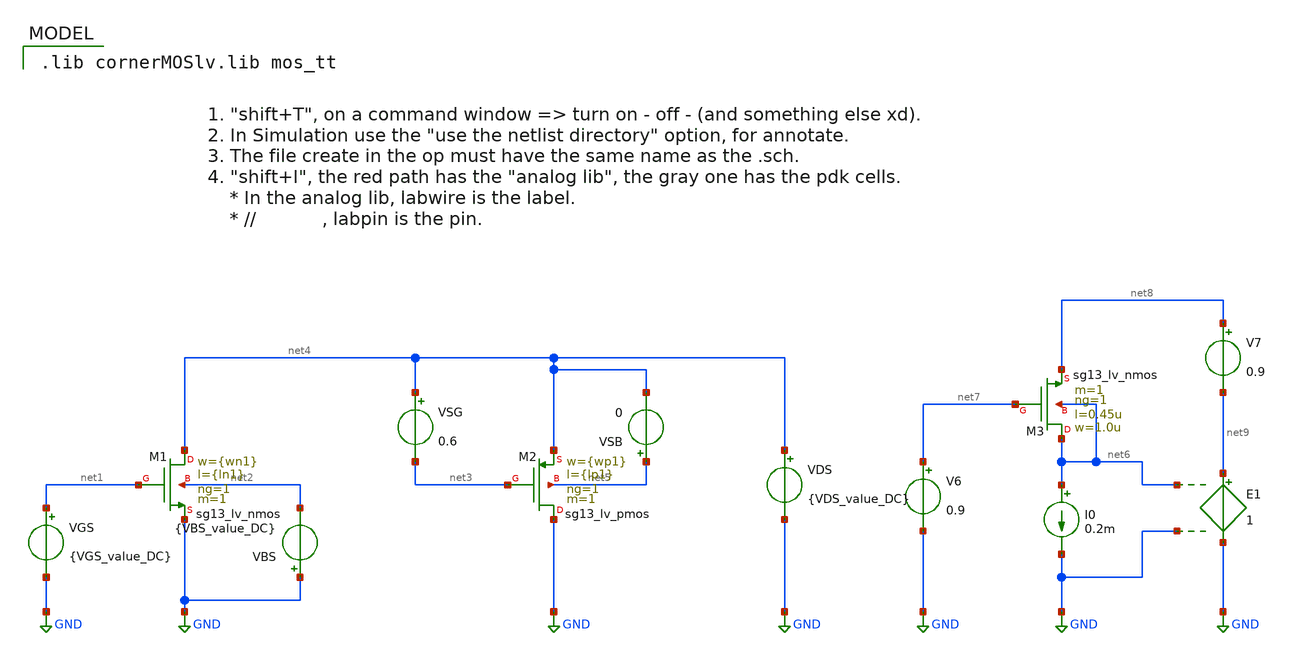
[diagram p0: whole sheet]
** sch_path: W2WDAC/W2W-DAC/CMOSCHART_sg130_lv_tb.sch
**.subckt CMOSCHART_sg130_lv_tb
VGS net1 GND {VGS_value_DC}
VDS net4 GND {VDS_value_DC}
VBS GND net2 {VBS_value_DC}
VSG net4 net3 0.6
VSB net5 net4 0
I0 net6 GND 0.2m
V6 net7 GND 0.9
V7 net8 net9 0.9
E1 net9 GND net6 GND 1
XM1 net4 net1 GND net2 sg13_lv_nmos w={wn1} l={ln1} ng=1 m=1 mm_ok=1
XM2 GND net3 net4 net5 sg13_lv_pmos w={wp1} l={lp1} ng=1 m=1 mm_ok=1
XM3 net6 net7 net8 net6 sg13_lv_nmos w=1.0u l=0.45u ng=1 m=1 mm_ok=1
**** begin user architecture code
 .lib cornerMOSlv.lib mos_tt



.option sparse
.param wp1=1u
.param lp1=0.13u
.temp 65
.param wn1=1u
.param ln1=0.13u
.param VGS_value_DC=0.6
.param VDS_value_DC=0.6
.param VBS_value_DC=0

.op
.save all
.control
option numdgt=3
set wr_singlescale
set wr_vecnames

compose wp_vec start=1.44u stop=1.46u step=0.005u
*6u 6.5u 7u 7.5u 8u 8.5u 9u 9.5u 10u 10.5u 11u 11.5u 12u 12.5u 13u 13.5u 14u 14.5u 15u 15.5u 16u
*+ 16.5u 17u
*50u 55u 60u 65u 70u 75u 80u 85u 90u 95u 100u 105u 110u 115u 120u 125u 130u 135u 140u 145u 150u 155u
*+ 160u 165u 170u 175u 180u 185u 190u 195u 200u
*2u 2.5u 3u 3.5u 4u 4.5u 5u 5.5u 6u 6.5u 7u 7.5u 8u 8.5u 9u 9.5u 10u 10.5u 11u 11.5u 12u

foreach var1 $&wp_vec
  alterparam wp1 = $var1
  reset
  run
  let Vgsp = @n.xm2.nsg13_lv_pmos[vgs]
  let Vdsp = @n.xm2.nsg13_lv_pmos[vds]
  let idp = @n.xm2.nsg13_lv_pmos[ids]
  let vdsatp = @n.xm2.nsg13_lv_pmos[vsat]
  let vthp = @n.xm2.nsg13_lv_pmos[vth]
  let rop = @n.xm2.nsg13_lv_pmos[gds]
  let cggp = @n.xm2.nsg13_lv_pmos[cgg]
  let Vovp = Vgsp - vthp
  let deltaVdsp = Vdsp - vdsatp
  let wp = @n.xm2.nsg13_lv_pmos[w]
  print wp Vgsp Vdsp idp vdsatp vthp deltaVdsp Vovp rop cggp
  destroy all
  set appendwrite
  unset set wr_vecnames
end

set appendwrite=0

alterparam wp1=0.1u

reset

write CMOSCHART_sg130_lv_tb.raw
set appendwrite


.endc


**** end user architecture code
**.ends
.GLOBAL GND
.end
